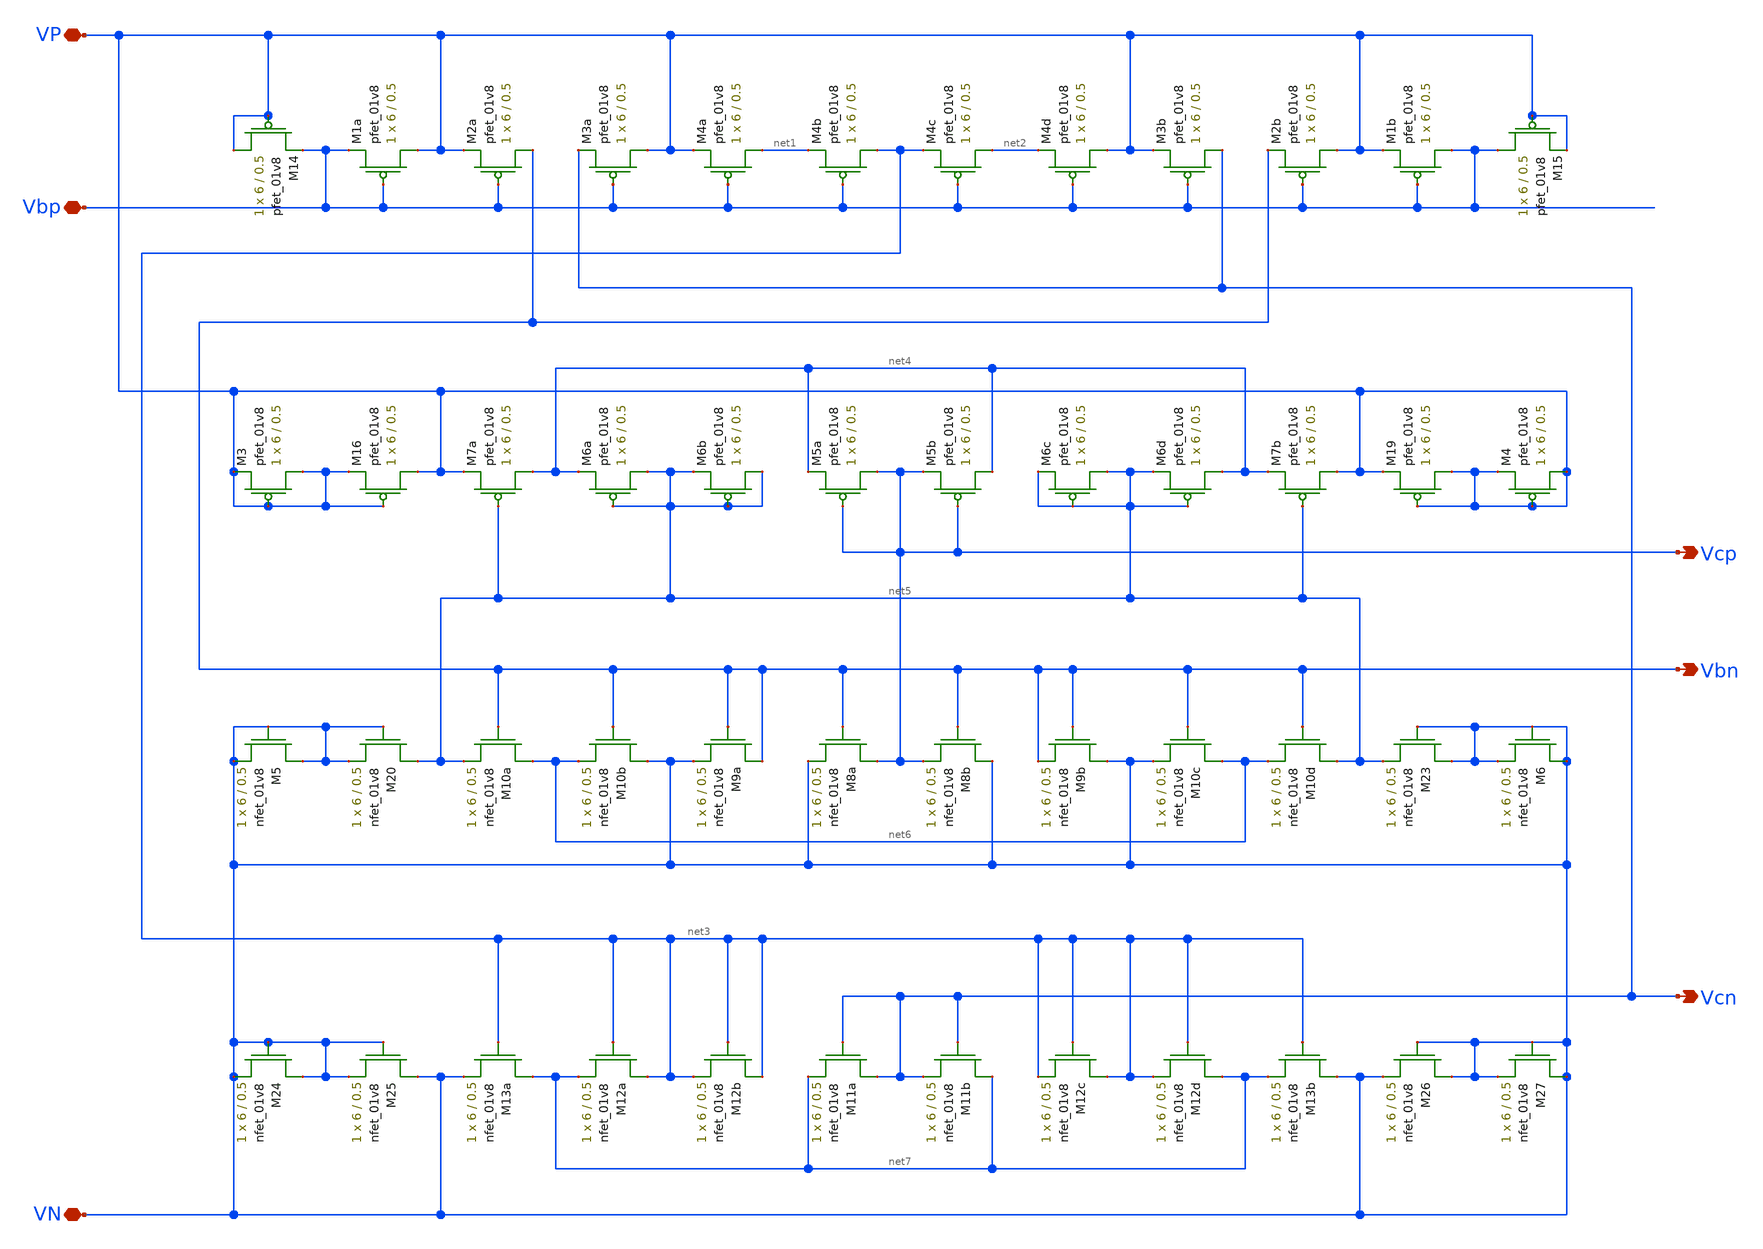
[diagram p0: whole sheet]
** sch_path: schematic/cascode_bias_LDS.sch
**.subckt cascode_bias_LDS VP VN Vcp Vbn Vcn Vbp
*.iopin VP
*.iopin VN
*.opin Vcp
*.opin Vbn
*.opin Vcn
*.iopin Vbp
XM1a VP Vbp Vbp VDD sky130_fd_pr__pfet_01v8 L=0.5 W=6 nf=1 ad='int((nf+1)/2) * W/nf * 0.29' as='int((nf+2)/2) * W/nf * 0.29'
+ pd='2*int((nf+1)/2) * (W/nf + 0.29)' ps='2*int((nf+2)/2) * (W/nf + 0.29)' nrd='0.29 / W' nrs='0.29 / W'
+ sa=0 sb=0 sd=0 mult=1 m=1
XM2a Vbn Vbp VP VDD sky130_fd_pr__pfet_01v8 L=0.5 W=6 nf=1 ad='int((nf+1)/2) * W/nf * 0.29' as='int((nf+2)/2) * W/nf * 0.29'
+ pd='2*int((nf+1)/2) * (W/nf + 0.29)' ps='2*int((nf+2)/2) * (W/nf + 0.29)' nrd='0.29 / W' nrs='0.29 / W'
+ sa=0 sb=0 sd=0 mult=1 m=1
XM3a VP Vbp Vcn VDD sky130_fd_pr__pfet_01v8 L=0.5 W=6 nf=1 ad='int((nf+1)/2) * W/nf * 0.29' as='int((nf+2)/2) * W/nf * 0.29'
+ pd='2*int((nf+1)/2) * (W/nf + 0.29)' ps='2*int((nf+2)/2) * (W/nf + 0.29)' nrd='0.29 / W' nrs='0.29 / W'
+ sa=0 sb=0 sd=0 mult=1 m=1
XM4a net1 Vbp VP VDD sky130_fd_pr__pfet_01v8 L=0.5 W=6 nf=1 ad='int((nf+1)/2) * W/nf * 0.29' as='int((nf+2)/2) * W/nf * 0.29'
+ pd='2*int((nf+1)/2) * (W/nf + 0.29)' ps='2*int((nf+2)/2) * (W/nf + 0.29)' nrd='0.29 / W' nrs='0.29 / W'
+ sa=0 sb=0 sd=0 mult=1 m=1
XM4c net2 Vbp net3 VDD sky130_fd_pr__pfet_01v8 L=0.5 W=6 nf=1 ad='int((nf+1)/2) * W/nf * 0.29' as='int((nf+2)/2) * W/nf * 0.29'
+ pd='2*int((nf+1)/2) * (W/nf + 0.29)' ps='2*int((nf+2)/2) * (W/nf + 0.29)' nrd='0.29 / W' nrs='0.29 / W'
+ sa=0 sb=0 sd=0 mult=1 m=1
XM3b Vcn Vbp VP VDD sky130_fd_pr__pfet_01v8 L=0.5 W=6 nf=1 ad='int((nf+1)/2) * W/nf * 0.29' as='int((nf+2)/2) * W/nf * 0.29'
+ pd='2*int((nf+1)/2) * (W/nf + 0.29)' ps='2*int((nf+2)/2) * (W/nf + 0.29)' nrd='0.29 / W' nrs='0.29 / W'
+ sa=0 sb=0 sd=0 mult=1 m=1
XM2b VP Vbp Vbn VDD sky130_fd_pr__pfet_01v8 L=0.5 W=6 nf=1 ad='int((nf+1)/2) * W/nf * 0.29' as='int((nf+2)/2) * W/nf * 0.29'
+ pd='2*int((nf+1)/2) * (W/nf + 0.29)' ps='2*int((nf+2)/2) * (W/nf + 0.29)' nrd='0.29 / W' nrs='0.29 / W'
+ sa=0 sb=0 sd=0 mult=1 m=1
XM1b Vbp Vbp VP VDD sky130_fd_pr__pfet_01v8 L=0.5 W=6 nf=1 ad='int((nf+1)/2) * W/nf * 0.29' as='int((nf+2)/2) * W/nf * 0.29'
+ pd='2*int((nf+1)/2) * (W/nf + 0.29)' ps='2*int((nf+2)/2) * (W/nf + 0.29)' nrd='0.29 / W' nrs='0.29 / W'
+ sa=0 sb=0 sd=0 mult=1 m=1
XM6a net5 net5 net4 VDD sky130_fd_pr__pfet_01v8 L=0.5 W=6 nf=1 ad='int((nf+1)/2) * W/nf * 0.29' as='int((nf+2)/2) * W/nf * 0.29'
+ pd='2*int((nf+1)/2) * (W/nf + 0.29)' ps='2*int((nf+2)/2) * (W/nf + 0.29)' nrd='0.29 / W' nrs='0.29 / W'
+ sa=0 sb=0 sd=0 mult=1 m=1
XM6b net5 net5 net5 VDD sky130_fd_pr__pfet_01v8 L=0.5 W=6 nf=1 ad='int((nf+1)/2) * W/nf * 0.29' as='int((nf+2)/2) * W/nf * 0.29'
+ pd='2*int((nf+1)/2) * (W/nf + 0.29)' ps='2*int((nf+2)/2) * (W/nf + 0.29)' nrd='0.29 / W' nrs='0.29 / W'
+ sa=0 sb=0 sd=0 mult=1 m=1
XM5a Vcp Vcp net4 VDD sky130_fd_pr__pfet_01v8 L=0.5 W=6 nf=1 ad='int((nf+1)/2) * W/nf * 0.29' as='int((nf+2)/2) * W/nf * 0.29'
+ pd='2*int((nf+1)/2) * (W/nf + 0.29)' ps='2*int((nf+2)/2) * (W/nf + 0.29)' nrd='0.29 / W' nrs='0.29 / W'
+ sa=0 sb=0 sd=0 mult=1 m=1
XM5b net4 Vcp Vcp VDD sky130_fd_pr__pfet_01v8 L=0.5 W=6 nf=1 ad='int((nf+1)/2) * W/nf * 0.29' as='int((nf+2)/2) * W/nf * 0.29'
+ pd='2*int((nf+1)/2) * (W/nf + 0.29)' ps='2*int((nf+2)/2) * (W/nf + 0.29)' nrd='0.29 / W' nrs='0.29 / W'
+ sa=0 sb=0 sd=0 mult=1 m=1
XM6c net5 net5 net5 VDD sky130_fd_pr__pfet_01v8 L=0.5 W=6 nf=1 ad='int((nf+1)/2) * W/nf * 0.29' as='int((nf+2)/2) * W/nf * 0.29'
+ pd='2*int((nf+1)/2) * (W/nf + 0.29)' ps='2*int((nf+2)/2) * (W/nf + 0.29)' nrd='0.29 / W' nrs='0.29 / W'
+ sa=0 sb=0 sd=0 mult=1 m=1
XM6d net4 net5 net5 VDD sky130_fd_pr__pfet_01v8 L=0.5 W=6 nf=1 ad='int((nf+1)/2) * W/nf * 0.29' as='int((nf+2)/2) * W/nf * 0.29'
+ pd='2*int((nf+1)/2) * (W/nf + 0.29)' ps='2*int((nf+2)/2) * (W/nf + 0.29)' nrd='0.29 / W' nrs='0.29 / W'
+ sa=0 sb=0 sd=0 mult=1 m=1
XM8a Vcp Vbn VN GND sky130_fd_pr__nfet_01v8 L=0.5 W=6 nf=1 ad='int((nf+1)/2) * W/nf * 0.29' as='int((nf+2)/2) * W/nf * 0.29'
+ pd='2*int((nf+1)/2) * (W/nf + 0.29)' ps='2*int((nf+2)/2) * (W/nf + 0.29)' nrd='0.29 / W' nrs='0.29 / W'
+ sa=0 sb=0 sd=0 mult=1 m=1
XM8b VN Vbn Vcp GND sky130_fd_pr__nfet_01v8 L=0.5 W=6 nf=1 ad='int((nf+1)/2) * W/nf * 0.29' as='int((nf+2)/2) * W/nf * 0.29'
+ pd='2*int((nf+1)/2) * (W/nf + 0.29)' ps='2*int((nf+2)/2) * (W/nf + 0.29)' nrd='0.29 / W' nrs='0.29 / W'
+ sa=0 sb=0 sd=0 mult=1 m=1
XM10b VN Vbn net6 GND sky130_fd_pr__nfet_01v8 L=0.5 W=6 nf=1 ad='int((nf+1)/2) * W/nf * 0.29' as='int((nf+2)/2) * W/nf * 0.29'
+ pd='2*int((nf+1)/2) * (W/nf + 0.29)' ps='2*int((nf+2)/2) * (W/nf + 0.29)' nrd='0.29 / W' nrs='0.29 / W'
+ sa=0 sb=0 sd=0 mult=1 m=1
XM9a Vbn Vbn VN GND sky130_fd_pr__nfet_01v8 L=0.5 W=6 nf=1 ad='int((nf+1)/2) * W/nf * 0.29' as='int((nf+2)/2) * W/nf * 0.29'
+ pd='2*int((nf+1)/2) * (W/nf + 0.29)' ps='2*int((nf+2)/2) * (W/nf + 0.29)' nrd='0.29 / W' nrs='0.29 / W'
+ sa=0 sb=0 sd=0 mult=1 m=1
XM9b VN Vbn Vbn GND sky130_fd_pr__nfet_01v8 L=0.5 W=6 nf=1 ad='int((nf+1)/2) * W/nf * 0.29' as='int((nf+2)/2) * W/nf * 0.29'
+ pd='2*int((nf+1)/2) * (W/nf + 0.29)' ps='2*int((nf+2)/2) * (W/nf + 0.29)' nrd='0.29 / W' nrs='0.29 / W'
+ sa=0 sb=0 sd=0 mult=1 m=1
XM10c net6 Vbn VN GND sky130_fd_pr__nfet_01v8 L=0.5 W=6 nf=1 ad='int((nf+1)/2) * W/nf * 0.29' as='int((nf+2)/2) * W/nf * 0.29'
+ pd='2*int((nf+1)/2) * (W/nf + 0.29)' ps='2*int((nf+2)/2) * (W/nf + 0.29)' nrd='0.29 / W' nrs='0.29 / W'
+ sa=0 sb=0 sd=0 mult=1 m=1
XM11a Vcn Vcn net7 GND sky130_fd_pr__nfet_01v8 L=0.5 W=6 nf=1 ad='int((nf+1)/2) * W/nf * 0.29' as='int((nf+2)/2) * W/nf * 0.29'
+ pd='2*int((nf+1)/2) * (W/nf + 0.29)' ps='2*int((nf+2)/2) * (W/nf + 0.29)' nrd='0.29 / W' nrs='0.29 / W'
+ sa=0 sb=0 sd=0 mult=1 m=1
XM11b net7 Vcn Vcn GND sky130_fd_pr__nfet_01v8 L=0.5 W=6 nf=1 ad='int((nf+1)/2) * W/nf * 0.29' as='int((nf+2)/2) * W/nf * 0.29'
+ pd='2*int((nf+1)/2) * (W/nf + 0.29)' ps='2*int((nf+2)/2) * (W/nf + 0.29)' nrd='0.29 / W' nrs='0.29 / W'
+ sa=0 sb=0 sd=0 mult=1 m=1
XM13a net7 net3 VN GND sky130_fd_pr__nfet_01v8 L=0.5 W=6 nf=1 ad='int((nf+1)/2) * W/nf * 0.29' as='int((nf+2)/2) * W/nf * 0.29'
+ pd='2*int((nf+1)/2) * (W/nf + 0.29)' ps='2*int((nf+2)/2) * (W/nf + 0.29)' nrd='0.29 / W' nrs='0.29 / W'
+ sa=0 sb=0 sd=0 mult=1 m=1
XM12a net3 net3 net7 GND sky130_fd_pr__nfet_01v8 L=0.5 W=6 nf=1 ad='int((nf+1)/2) * W/nf * 0.29' as='int((nf+2)/2) * W/nf * 0.29'
+ pd='2*int((nf+1)/2) * (W/nf + 0.29)' ps='2*int((nf+2)/2) * (W/nf + 0.29)' nrd='0.29 / W' nrs='0.29 / W'
+ sa=0 sb=0 sd=0 mult=1 m=1
XM12d net7 net3 net3 GND sky130_fd_pr__nfet_01v8 L=0.5 W=6 nf=1 ad='int((nf+1)/2) * W/nf * 0.29' as='int((nf+2)/2) * W/nf * 0.29'
+ pd='2*int((nf+1)/2) * (W/nf + 0.29)' ps='2*int((nf+2)/2) * (W/nf + 0.29)' nrd='0.29 / W' nrs='0.29 / W'
+ sa=0 sb=0 sd=0 mult=1 m=1
XM13b VN net3 net7 GND sky130_fd_pr__nfet_01v8 L=0.5 W=6 nf=1 ad='int((nf+1)/2) * W/nf * 0.29' as='int((nf+2)/2) * W/nf * 0.29'
+ pd='2*int((nf+1)/2) * (W/nf + 0.29)' ps='2*int((nf+2)/2) * (W/nf + 0.29)' nrd='0.29 / W' nrs='0.29 / W'
+ sa=0 sb=0 sd=0 mult=1 m=1
XM15 Vbp VP VP VDD sky130_fd_pr__pfet_01v8 L=0.5 W=6 nf=1 ad='int((nf+1)/2) * W/nf * 0.29' as='int((nf+2)/2) * W/nf * 0.29'
+ pd='2*int((nf+1)/2) * (W/nf + 0.29)' ps='2*int((nf+2)/2) * (W/nf + 0.29)' nrd='0.29 / W' nrs='0.29 / W'
+ sa=0 sb=0 sd=0 mult=1 m=1
XM25 VN VN VN GND sky130_fd_pr__nfet_01v8 L=0.5 W=6 nf=1 ad='int((nf+1)/2) * W/nf * 0.29' as='int((nf+2)/2) * W/nf * 0.29'
+ pd='2*int((nf+1)/2) * (W/nf + 0.29)' ps='2*int((nf+2)/2) * (W/nf + 0.29)' nrd='0.29 / W' nrs='0.29 / W'
+ sa=0 sb=0 sd=0 mult=1 m=1
XM24 VN VN VN GND sky130_fd_pr__nfet_01v8 L=0.5 W=6 nf=1 ad='int((nf+1)/2) * W/nf * 0.29' as='int((nf+2)/2) * W/nf * 0.29'
+ pd='2*int((nf+1)/2) * (W/nf + 0.29)' ps='2*int((nf+2)/2) * (W/nf + 0.29)' nrd='0.29 / W' nrs='0.29 / W'
+ sa=0 sb=0 sd=0 mult=1 m=1
XM26 VN VN VN GND sky130_fd_pr__nfet_01v8 L=0.5 W=6 nf=1 ad='int((nf+1)/2) * W/nf * 0.29' as='int((nf+2)/2) * W/nf * 0.29'
+ pd='2*int((nf+1)/2) * (W/nf + 0.29)' ps='2*int((nf+2)/2) * (W/nf + 0.29)' nrd='0.29 / W' nrs='0.29 / W'
+ sa=0 sb=0 sd=0 mult=1 m=1
XM27 VN VN VN GND sky130_fd_pr__nfet_01v8 L=0.5 W=6 nf=1 ad='int((nf+1)/2) * W/nf * 0.29' as='int((nf+2)/2) * W/nf * 0.29'
+ pd='2*int((nf+1)/2) * (W/nf + 0.29)' ps='2*int((nf+2)/2) * (W/nf + 0.29)' nrd='0.29 / W' nrs='0.29 / W'
+ sa=0 sb=0 sd=0 mult=1 m=1
XM10a net6 Vbn net5 GND sky130_fd_pr__nfet_01v8 L=0.5 W=6 nf=1 ad='int((nf+1)/2) * W/nf * 0.29' as='int((nf+2)/2) * W/nf * 0.29'
+ pd='2*int((nf+1)/2) * (W/nf + 0.29)' ps='2*int((nf+2)/2) * (W/nf + 0.29)' nrd='0.29 / W' nrs='0.29 / W'
+ sa=0 sb=0 sd=0 mult=1 m=1
XM20 net5 VN VN GND sky130_fd_pr__nfet_01v8 L=0.5 W=6 nf=1 ad='int((nf+1)/2) * W/nf * 0.29' as='int((nf+2)/2) * W/nf * 0.29'
+ pd='2*int((nf+1)/2) * (W/nf + 0.29)' ps='2*int((nf+2)/2) * (W/nf + 0.29)' nrd='0.29 / W' nrs='0.29 / W'
+ sa=0 sb=0 sd=0 mult=1 m=1
XM23 VN VN net5 GND sky130_fd_pr__nfet_01v8 L=0.5 W=6 nf=1 ad='int((nf+1)/2) * W/nf * 0.29' as='int((nf+2)/2) * W/nf * 0.29'
+ pd='2*int((nf+1)/2) * (W/nf + 0.29)' ps='2*int((nf+2)/2) * (W/nf + 0.29)' nrd='0.29 / W' nrs='0.29 / W'
+ sa=0 sb=0 sd=0 mult=1 m=1
XM10d net5 Vbn net6 GND sky130_fd_pr__nfet_01v8 L=0.5 W=6 nf=1 ad='int((nf+1)/2) * W/nf * 0.29' as='int((nf+2)/2) * W/nf * 0.29'
+ pd='2*int((nf+1)/2) * (W/nf + 0.29)' ps='2*int((nf+2)/2) * (W/nf + 0.29)' nrd='0.29 / W' nrs='0.29 / W'
+ sa=0 sb=0 sd=0 mult=1 m=1
XM14 VP VP Vbp VDD sky130_fd_pr__pfet_01v8 L=0.5 W=6 nf=1 ad='int((nf+1)/2) * W/nf * 0.29' as='int((nf+2)/2) * W/nf * 0.29'
+ pd='2*int((nf+1)/2) * (W/nf + 0.29)' ps='2*int((nf+2)/2) * (W/nf + 0.29)' nrd='0.29 / W' nrs='0.29 / W'
+ sa=0 sb=0 sd=0 mult=1 m=1
XM7a net4 net5 VP VDD sky130_fd_pr__pfet_01v8 L=0.5 W=6 nf=1 ad='int((nf+1)/2) * W/nf * 0.29' as='int((nf+2)/2) * W/nf * 0.29'
+ pd='2*int((nf+1)/2) * (W/nf + 0.29)' ps='2*int((nf+2)/2) * (W/nf + 0.29)' nrd='0.29 / W' nrs='0.29 / W'
+ sa=0 sb=0 sd=0 mult=1 m=1
XM16 VP VP VP VDD sky130_fd_pr__pfet_01v8 L=0.5 W=6 nf=1 ad='int((nf+1)/2) * W/nf * 0.29' as='int((nf+2)/2) * W/nf * 0.29'
+ pd='2*int((nf+1)/2) * (W/nf + 0.29)' ps='2*int((nf+2)/2) * (W/nf + 0.29)' nrd='0.29 / W' nrs='0.29 / W'
+ sa=0 sb=0 sd=0 mult=1 m=1
XM7b VP net5 net4 VDD sky130_fd_pr__pfet_01v8 L=0.5 W=6 nf=1 ad='int((nf+1)/2) * W/nf * 0.29' as='int((nf+2)/2) * W/nf * 0.29'
+ pd='2*int((nf+1)/2) * (W/nf + 0.29)' ps='2*int((nf+2)/2) * (W/nf + 0.29)' nrd='0.29 / W' nrs='0.29 / W'
+ sa=0 sb=0 sd=0 mult=1 m=1
XM19 VP VP VP VDD sky130_fd_pr__pfet_01v8 L=0.5 W=6 nf=1 ad='int((nf+1)/2) * W/nf * 0.29' as='int((nf+2)/2) * W/nf * 0.29'
+ pd='2*int((nf+1)/2) * (W/nf + 0.29)' ps='2*int((nf+2)/2) * (W/nf + 0.29)' nrd='0.29 / W' nrs='0.29 / W'
+ sa=0 sb=0 sd=0 mult=1 m=1
XM4b net3 Vbp net1 VDD sky130_fd_pr__pfet_01v8 L=0.5 W=6 nf=1 ad='int((nf+1)/2) * W/nf * 0.29' as='int((nf+2)/2) * W/nf * 0.29'
+ pd='2*int((nf+1)/2) * (W/nf + 0.29)' ps='2*int((nf+2)/2) * (W/nf + 0.29)' nrd='0.29 / W' nrs='0.29 / W'
+ sa=0 sb=0 sd=0 mult=1 m=1
XM4d VP Vbp net2 VDD sky130_fd_pr__pfet_01v8 L=0.5 W=6 nf=1 ad='int((nf+1)/2) * W/nf * 0.29' as='int((nf+2)/2) * W/nf * 0.29'
+ pd='2*int((nf+1)/2) * (W/nf + 0.29)' ps='2*int((nf+2)/2) * (W/nf + 0.29)' nrd='0.29 / W' nrs='0.29 / W'
+ sa=0 sb=0 sd=0 mult=1 m=1
XM3 VP VP VP VDD sky130_fd_pr__pfet_01v8 L=0.5 W=6 nf=1 ad='int((nf+1)/2) * W/nf * 0.29' as='int((nf+2)/2) * W/nf * 0.29'
+ pd='2*int((nf+1)/2) * (W/nf + 0.29)' ps='2*int((nf+2)/2) * (W/nf + 0.29)' nrd='0.29 / W' nrs='0.29 / W'
+ sa=0 sb=0 sd=0 mult=1 m=1
XM4 VP VP VP VDD sky130_fd_pr__pfet_01v8 L=0.5 W=6 nf=1 ad='int((nf+1)/2) * W/nf * 0.29' as='int((nf+2)/2) * W/nf * 0.29'
+ pd='2*int((nf+1)/2) * (W/nf + 0.29)' ps='2*int((nf+2)/2) * (W/nf + 0.29)' nrd='0.29 / W' nrs='0.29 / W'
+ sa=0 sb=0 sd=0 mult=1 m=1
XM5 VN VN VN GND sky130_fd_pr__nfet_01v8 L=0.5 W=6 nf=1 ad='int((nf+1)/2) * W/nf * 0.29' as='int((nf+2)/2) * W/nf * 0.29'
+ pd='2*int((nf+1)/2) * (W/nf + 0.29)' ps='2*int((nf+2)/2) * (W/nf + 0.29)' nrd='0.29 / W' nrs='0.29 / W'
+ sa=0 sb=0 sd=0 mult=1 m=1
XM6 VN VN VN GND sky130_fd_pr__nfet_01v8 L=0.5 W=6 nf=1 ad='int((nf+1)/2) * W/nf * 0.29' as='int((nf+2)/2) * W/nf * 0.29'
+ pd='2*int((nf+1)/2) * (W/nf + 0.29)' ps='2*int((nf+2)/2) * (W/nf + 0.29)' nrd='0.29 / W' nrs='0.29 / W'
+ sa=0 sb=0 sd=0 mult=1 m=1
XM12c net3 net3 net3 GND sky130_fd_pr__nfet_01v8 L=0.5 W=6 nf=1 ad='int((nf+1)/2) * W/nf * 0.29' as='int((nf+2)/2) * W/nf * 0.29'
+ pd='2*int((nf+1)/2) * (W/nf + 0.29)' ps='2*int((nf+2)/2) * (W/nf + 0.29)' nrd='0.29 / W' nrs='0.29 / W'
+ sa=0 sb=0 sd=0 mult=1 m=1
XM12b net3 net3 net3 GND sky130_fd_pr__nfet_01v8 L=0.5 W=6 nf=1 ad='int((nf+1)/2) * W/nf * 0.29' as='int((nf+2)/2) * W/nf * 0.29'
+ pd='2*int((nf+1)/2) * (W/nf + 0.29)' ps='2*int((nf+2)/2) * (W/nf + 0.29)' nrd='0.29 / W' nrs='0.29 / W'
+ sa=0 sb=0 sd=0 mult=1 m=1
**.ends
.end
